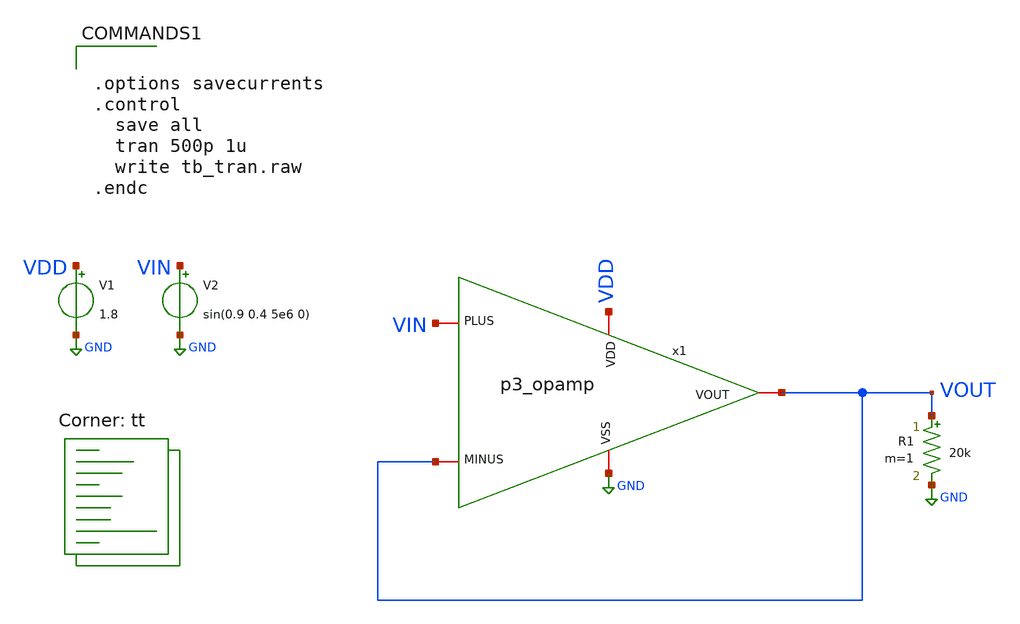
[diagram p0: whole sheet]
** sch_path: xschem/tb_p3_trans.sch
**.subckt tb_p3_trans
V1 VDD GND 1.8
V2 VIN GND sin(0.9 0.4 5e6 0)
R1 VOUT GND 20k m=1
x1 VDD VOUT VIN VOUT GND p3_opamp
**** begin user architecture code
.lib $::SKYWATER_MODELS/sky130.lib.spice tt


.options savecurrents
.control
  save all
  tran 500p 1u
  write tb_tran.raw
.endc


**** end user architecture code
**.ends

* expanding   symbol:  p3_opamp.sym # of pins=5
** sym_path: p3_opamp.sym
** sch_path: p3_opamp.sch
.subckt p3_opamp VDD MINUS PLUS VOUT VSS
*.iopin VDD
*.iopin VSS
*.iopin PLUS
*.iopin MINUS
*.iopin VOUT
XM3 VX VBIAS VSS VSS sky130_fd_pr__nfet_01v8 L=2 W=4 nf=4 ad='int((nf+1)/2) * W/nf * 0.29' as='int((nf+2)/2) * W/nf * 0.29'
+ pd='2*int((nf+1)/2) * (W/nf + 0.29)' ps='2*int((nf+2)/2) * (W/nf + 0.29)' nrd='0.29 / W' nrs='0.29 / W'
+ sa=0 sb=0 sd=0 mult=1 m=1
XM6 VBIAS VBIAS VSS VSS sky130_fd_pr__nfet_01v8 L=2 W=4 nf=4 ad='int((nf+1)/2) * W/nf * 0.29' as='int((nf+2)/2) * W/nf * 0.29'
+ pd='2*int((nf+1)/2) * (W/nf + 0.29)' ps='2*int((nf+2)/2) * (W/nf + 0.29)' nrd='0.29 / W' nrs='0.29 / W'
+ sa=0 sb=0 sd=0 mult=1 m=1
XM7 VOUT VBIAS VSS VSS sky130_fd_pr__nfet_01v8 L=2 W=7 nf=7 ad='int((nf+1)/2) * W/nf * 0.29' as='int((nf+2)/2) * W/nf * 0.29'
+ pd='2*int((nf+1)/2) * (W/nf + 0.29)' ps='2*int((nf+2)/2) * (W/nf + 0.29)' nrd='0.29 / W' nrs='0.29 / W'
+ sa=0 sb=0 sd=0 mult=1 m=1
XR1 VBIAS VDD VSS sky130_fd_pr__res_xhigh_po_0p35 L=2.9 mult=1 m=1
XM2 V2 MINUS VX VSS sky130_fd_pr__nfet_01v8_lvt L=0.5 W=2.5 nf=1 ad='int((nf+1)/2) * W/nf * 0.29' as='int((nf+2)/2) * W/nf * 0.29'
+ pd='2*int((nf+1)/2) * (W/nf + 0.29)' ps='2*int((nf+2)/2) * (W/nf + 0.29)' nrd='0.29 / W' nrs='0.29 / W'
+ sa=0 sb=0 sd=0 mult=1 m=1
XM1 V1 PLUS VX VSS sky130_fd_pr__nfet_01v8_lvt L=0.5 W=2.5 nf=1 ad='int((nf+1)/2) * W/nf * 0.29' as='int((nf+2)/2) * W/nf * 0.29'
+ pd='2*int((nf+1)/2) * (W/nf + 0.29)' ps='2*int((nf+2)/2) * (W/nf + 0.29)' nrd='0.29 / W' nrs='0.29 / W'
+ sa=0 sb=0 sd=0 mult=1 m=1
XM4 V2 V2 VDD VDD sky130_fd_pr__pfet_01v8_lvt L=2 W=6 nf=6 ad='int((nf+1)/2) * W/nf * 0.29' as='int((nf+2)/2) * W/nf * 0.29'
+ pd='2*int((nf+1)/2) * (W/nf + 0.29)' ps='2*int((nf+2)/2) * (W/nf + 0.29)' nrd='0.29 / W' nrs='0.29 / W'
+ sa=0 sb=0 sd=0 mult=1 m=1
XM5 V1 V2 VDD VDD sky130_fd_pr__pfet_01v8_lvt L=2 W=6 nf=6 ad='int((nf+1)/2) * W/nf * 0.29' as='int((nf+2)/2) * W/nf * 0.29'
+ pd='2*int((nf+1)/2) * (W/nf + 0.29)' ps='2*int((nf+2)/2) * (W/nf + 0.29)' nrd='0.29 / W' nrs='0.29 / W'
+ sa=0 sb=0 sd=0 mult=1 m=1
XM8 VOUT V1 VDD VDD sky130_fd_pr__pfet_01v8_lvt L=0.5 W=20 nf=20 ad='int((nf+1)/2) * W/nf * 0.29' as='int((nf+2)/2) * W/nf * 0.29'
+ pd='2*int((nf+1)/2) * (W/nf + 0.29)' ps='2*int((nf+2)/2) * (W/nf + 0.29)' nrd='0.29 / W' nrs='0.29 / W'
+ sa=0 sb=0 sd=0 mult=1 m=1
.ends

.GLOBAL GND
.end
